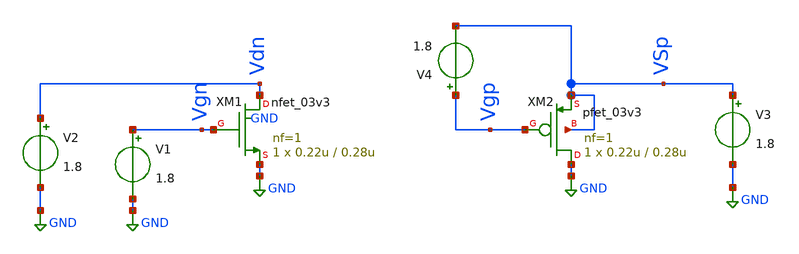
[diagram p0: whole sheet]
** sch_path: xschem/caracterizador/charac.sch
* Copyright 2022 GlobalFoundries PDK Authors
* Licensed under the Apache License, Version 2.0 (the "License");
* you may not use this file except in compliance with the License.
* You may obtain a copy of the License at
* https://www.apache.org/licenses/LICENSE-2.0
* Unless required by applicable law or agreed to in writing, software
* distributed under the License is distributed on an "AS IS" BASIS,
* WITHOUT WARRANTIES OR CONDITIONS OF ANY KIND, either express or implied.
* See the License for the specific language governing permissions and
* limitations under the License.
**.subckt charac
XM1 Vdn Vgn GND GND nfet_03v3 L=0.28u W=0.22u nf=1 ad='int((nf+1)/2) * W/nf * 0.18u' as='int((nf+2)/2) * W/nf * 0.18u'
+ pd='2*int((nf+1)/2) * (W/nf + 0.18u)' ps='2*int((nf+2)/2) * (W/nf + 0.18u)' nrd='0.18u / W' nrs='0.18u / W'
+ sa=0 sb=0 sd=0 m=1 par=1
XM2 GND Vgp VSp VSp pfet_03v3 L=0.28u W=0.22u nf=1 ad='int((nf+1)/2) * W/nf * 0.18u' as='int((nf+2)/2) * W/nf * 0.18u'
+ pd='2*int((nf+1)/2) * (W/nf + 0.18u)' ps='2*int((nf+2)/2) * (W/nf + 0.18u)' nrd='0.18u / W' nrs='0.18u / W'
+ sa=0 sb=0 sd=0 m=1 par=1
V1 Vgn GND 1.8
V2 Vdn GND 1.8
V3 VSp GND 1.8
V4 Vgp VSp 1.8
**** begin user architecture code



.control
  save all

  * ===== NMOS =====
  dc V2 0 3.3 0.01 V1 0 3.3 0.55
  plot -i(V2) title 'NMOS Output' xlabel 'VDS' ylabel 'ID'

  dc V1 0 3.3 0.01 V2 0.55 3.3 0.55
  plot -i(V2) title 'NMOS Transfer' xlabel 'VGS' ylabel 'ID'

  alter V2 = 1.65
  dc V1 0 3.3 0.01
  let idn = -i(V2)
  let gmn = deriv(idn)
  let gmidn = gmn/idn
  plot gmidn vs idn xlog xlimit 1e-9 1e-3 ylimit 0 35 title 'NMOS gm/Id' xlabel 'ID' ylabel 'gm/ID (1/V)'

  * ===== PMOS (V3 = VSD, V4 = VGS negativo, referido a la fuente) =====
  dc V3 0 3.3 0.01 V4 0 -3.3 -0.55
  plot -i(V3) title 'PMOS Output' xlabel 'VSD' ylabel '|ID|'

  dc V4 0 -3.3 -0.01 V3 0.55 3.3 0.55
  plot -i(V3) title 'PMOS Transfer' xlabel 'VGS' ylabel '|ID|'

  alter V3 = 1.65
  dc V4 0 -3.3 -0.01
  let idp = -i(V3)
  let gmp = abs(deriv(idp))
  let gmidp = gmp/idp
  plot gmidp vs idp xlog xlimit 1e-9 1e-3 ylimit 0 35 title 'PMOS gm/Id' xlabel '|ID| (A)' ylabel 'gm/ID (1/V)'
.endc




.include /home/ringosinye/eda/pdks/gf180mcuD/libs.tech/ngspice/design.ngspice
.lib /home/ringosinye/eda/pdks/gf180mcuD/libs.tech/ngspice/sm141064.ngspice typical


**** end user architecture code
**.ends
.GLOBAL GND
.end
